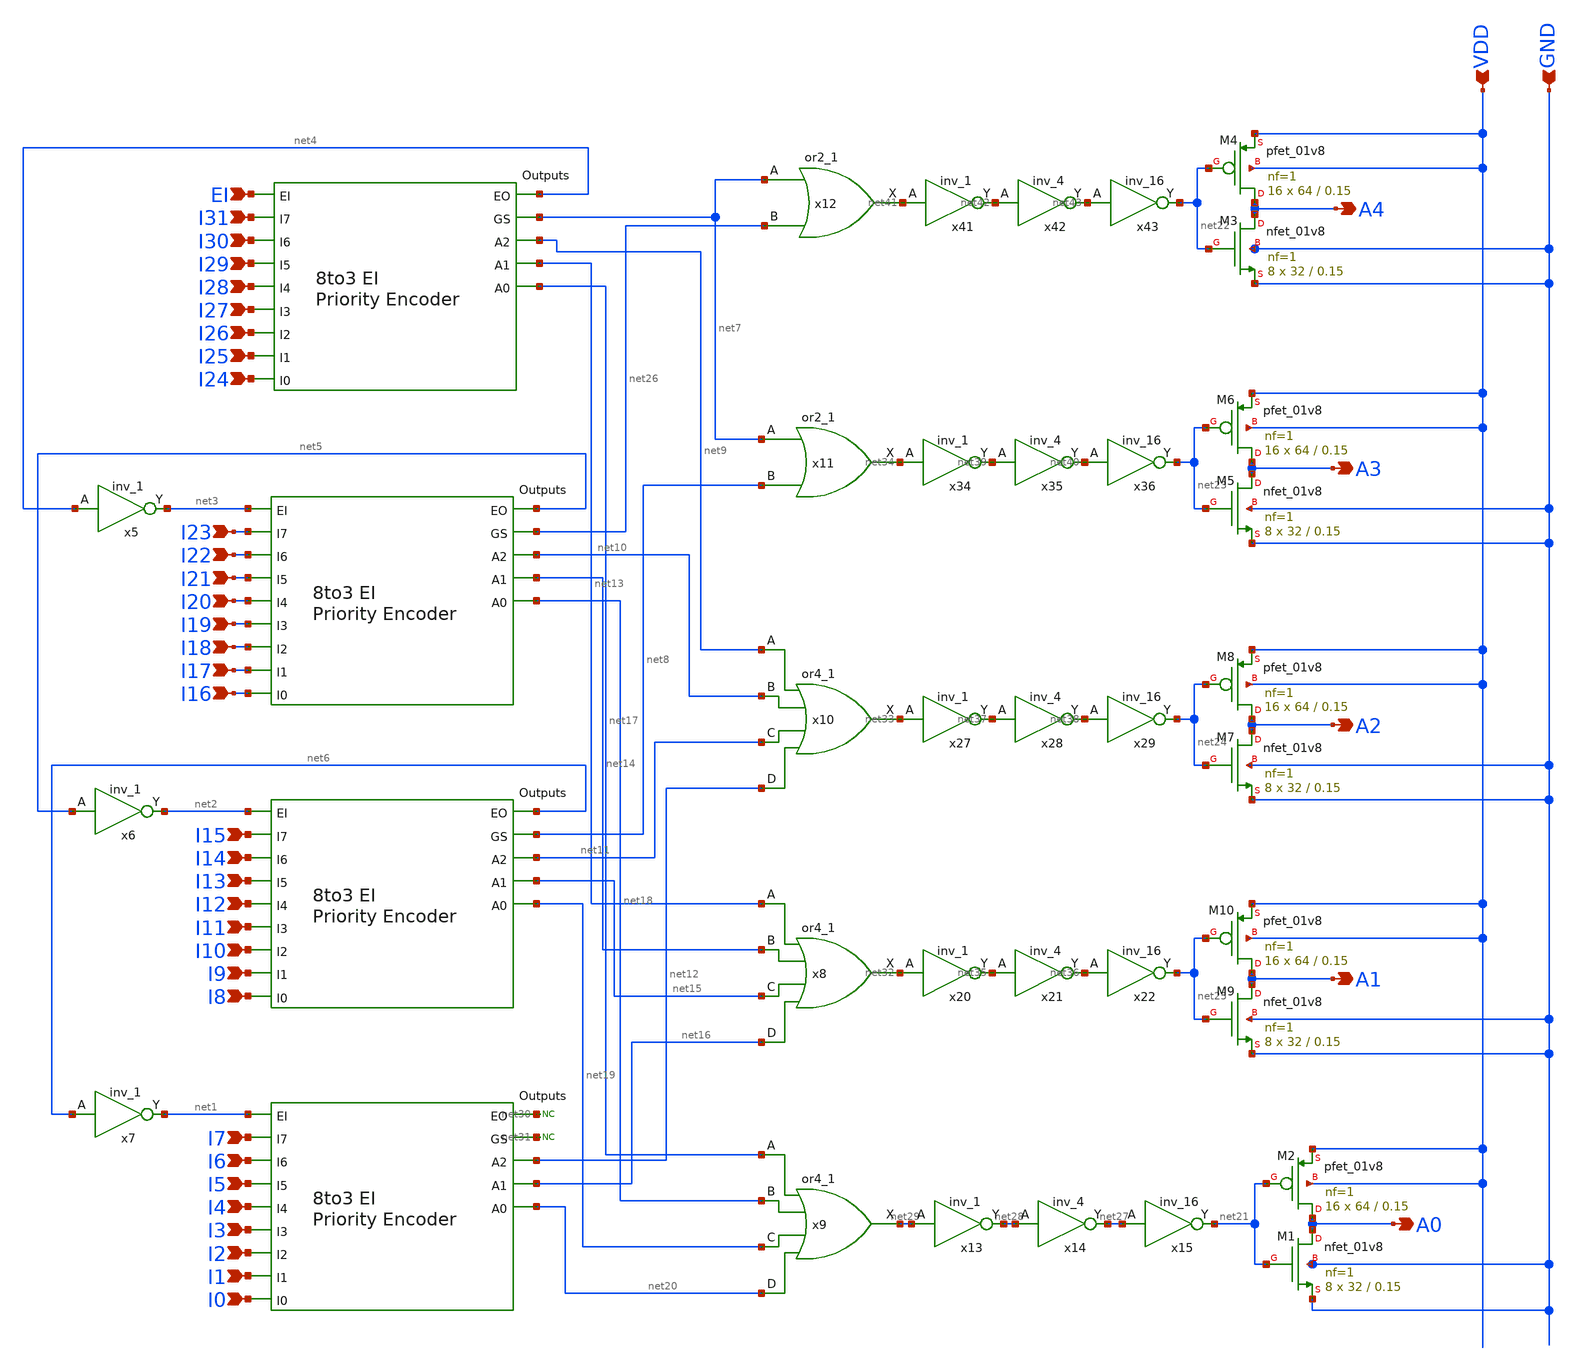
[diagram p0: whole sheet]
** sch_path: PriorityEncoder/xschem/32to5_Priority_Encoder_v0p2p1.sch
.lib $::SKYWATER_MODELS/sky130.lib.spice tt
.include $::SKYWATER_STDCELLS/sky130_fd_sc_hd.spice

**.subckt 32to5_Priority_Encoder_v0p2p1 EI I31 I30 I29 I28 I27 I26 I25 I24 I23 I22 I21 I20 I19 I18
*+ I17 I16 I15 I14 I13 I12 I11 I10 I9 I8 I7 I6 I5 I4 I3 I2 I1 I0 A0 A4 A3 A2 A1 VDD GND
*.ipin EI
*.ipin I31
*.ipin I30
*.ipin I29
*.ipin I28
*.ipin I27
*.ipin I26
*.ipin I25
*.ipin I24
*.ipin I23
*.ipin I22
*.ipin I21
*.ipin I20
*.ipin I19
*.ipin I18
*.ipin I17
*.ipin I16
*.ipin I15
*.ipin I14
*.ipin I13
*.ipin I12
*.ipin I11
*.ipin I10
*.ipin I9
*.ipin I8
*.ipin I7
*.ipin I6
*.ipin I5
*.ipin I4
*.ipin I3
*.ipin I2
*.ipin I1
*.ipin I0
*.opin A0
*.opin A4
*.opin A3
*.opin A2
*.opin A1
*.ipin VDD
*.ipin GND
x1 I25 I29 I27 I24 I26 I30 I31 I28 net4 net7 net9 net13 net17 EI 8to3_Priority_Encoder_v0p2p0
x2 I17 I21 I19 I16 I18 I22 I23 I20 net5 net26 net10 net14 net18 net3 8to3_Priority_Encoder_v0p2p0
x3 I9 I13 I11 I8 I10 I14 I15 I12 net6 net8 net11 net15 net19 net2 8to3_Priority_Encoder_v0p2p0
x4 I1 I5 I3 I0 I2 I6 I7 I4 net30 net31 net12 net16 net20 net1 8to3_Priority_Encoder_v0p2p0
x5 net4 GND GND VDD VDD net3 sky130_fd_sc_hd__inv_1
x9 net17 net18 net19 net20 GND GND VDD VDD net29 sky130_fd_sc_hd__or4_1
x8 net13 net14 net15 net16 GND GND VDD VDD net32 sky130_fd_sc_hd__or4_1
x10 net9 net10 net11 net12 GND GND VDD VDD net33 sky130_fd_sc_hd__or4_1
x11 net7 net8 GND GND VDD VDD net34 sky130_fd_sc_hd__or2_1
x13 net29 GND GND VDD VDD net28 sky130_fd_sc_hd__inv_1
x14 net28 GND GND VDD VDD net27 sky130_fd_sc_hd__inv_4
x15 net27 GND GND VDD VDD net21 sky130_fd_sc_hd__inv_16
x20 net32 GND GND VDD VDD net35 sky130_fd_sc_hd__inv_1
x21 net35 GND GND VDD VDD net36 sky130_fd_sc_hd__inv_4
x22 net36 GND GND VDD VDD net25 sky130_fd_sc_hd__inv_16
x27 net33 GND GND VDD VDD net37 sky130_fd_sc_hd__inv_1
x28 net37 GND GND VDD VDD net38 sky130_fd_sc_hd__inv_4
x29 net38 GND GND VDD VDD net24 sky130_fd_sc_hd__inv_16
x34 net34 GND GND VDD VDD net39 sky130_fd_sc_hd__inv_1
x35 net39 GND GND VDD VDD net40 sky130_fd_sc_hd__inv_4
x36 net40 GND GND VDD VDD net23 sky130_fd_sc_hd__inv_16
x12 net7 net26 GND GND VDD VDD net41 sky130_fd_sc_hd__or2_1
x41 net41 GND GND VDD VDD net42 sky130_fd_sc_hd__inv_1
x42 net42 GND GND VDD VDD net43 sky130_fd_sc_hd__inv_4
x43 net43 GND GND VDD VDD net22 sky130_fd_sc_hd__inv_16
* noconn #net30
* noconn #net31
XM3 A4 net22 GND GND sky130_fd_pr__nfet_01v8 L=0.15 W=32 nf=1 ad='int((nf+1)/2) * W/nf * 0.29' as='int((nf+2)/2) * W/nf * 0.29'
+ pd='2*int((nf+1)/2) * (W/nf + 0.29)' ps='2*int((nf+2)/2) * (W/nf + 0.29)' nrd='0.29 / W' nrs='0.29 / W'
+ sa=0 sb=0 sd=0 mult=8 m=8
XM4 A4 net22 VDD VDD sky130_fd_pr__pfet_01v8 L=0.15 W=64 nf=1 ad='int((nf+1)/2) * W/nf * 0.29' as='int((nf+2)/2) * W/nf * 0.29'
+ pd='2*int((nf+1)/2) * (W/nf + 0.29)' ps='2*int((nf+2)/2) * (W/nf + 0.29)' nrd='0.29 / W' nrs='0.29 / W'
+ sa=0 sb=0 sd=0 mult=16 m=16
XM5 A3 net23 GND GND sky130_fd_pr__nfet_01v8 L=0.15 W=32 nf=1 ad='int((nf+1)/2) * W/nf * 0.29' as='int((nf+2)/2) * W/nf * 0.29'
+ pd='2*int((nf+1)/2) * (W/nf + 0.29)' ps='2*int((nf+2)/2) * (W/nf + 0.29)' nrd='0.29 / W' nrs='0.29 / W'
+ sa=0 sb=0 sd=0 mult=8 m=8
XM6 A3 net23 VDD VDD sky130_fd_pr__pfet_01v8 L=0.15 W=64 nf=1 ad='int((nf+1)/2) * W/nf * 0.29' as='int((nf+2)/2) * W/nf * 0.29'
+ pd='2*int((nf+1)/2) * (W/nf + 0.29)' ps='2*int((nf+2)/2) * (W/nf + 0.29)' nrd='0.29 / W' nrs='0.29 / W'
+ sa=0 sb=0 sd=0 mult=16 m=16
XM7 A2 net24 GND GND sky130_fd_pr__nfet_01v8 L=0.15 W=32 nf=1 ad='int((nf+1)/2) * W/nf * 0.29' as='int((nf+2)/2) * W/nf * 0.29'
+ pd='2*int((nf+1)/2) * (W/nf + 0.29)' ps='2*int((nf+2)/2) * (W/nf + 0.29)' nrd='0.29 / W' nrs='0.29 / W'
+ sa=0 sb=0 sd=0 mult=8 m=8
XM8 A2 net24 VDD VDD sky130_fd_pr__pfet_01v8 L=0.15 W=64 nf=1 ad='int((nf+1)/2) * W/nf * 0.29' as='int((nf+2)/2) * W/nf * 0.29'
+ pd='2*int((nf+1)/2) * (W/nf + 0.29)' ps='2*int((nf+2)/2) * (W/nf + 0.29)' nrd='0.29 / W' nrs='0.29 / W'
+ sa=0 sb=0 sd=0 mult=16 m=16
XM9 A1 net25 GND GND sky130_fd_pr__nfet_01v8 L=0.15 W=32 nf=1 ad='int((nf+1)/2) * W/nf * 0.29' as='int((nf+2)/2) * W/nf * 0.29'
+ pd='2*int((nf+1)/2) * (W/nf + 0.29)' ps='2*int((nf+2)/2) * (W/nf + 0.29)' nrd='0.29 / W' nrs='0.29 / W'
+ sa=0 sb=0 sd=0 mult=8 m=8
XM10 A1 net25 VDD VDD sky130_fd_pr__pfet_01v8 L=0.15 W=64 nf=1 ad='int((nf+1)/2) * W/nf * 0.29' as='int((nf+2)/2) * W/nf * 0.29'
+ pd='2*int((nf+1)/2) * (W/nf + 0.29)' ps='2*int((nf+2)/2) * (W/nf + 0.29)' nrd='0.29 / W' nrs='0.29 / W'
+ sa=0 sb=0 sd=0 mult=16 m=16
XM1 A0 net21 GND GND sky130_fd_pr__nfet_01v8 L=0.15 W=32 nf=1 ad='int((nf+1)/2) * W/nf * 0.29' as='int((nf+2)/2) * W/nf * 0.29'
+ pd='2*int((nf+1)/2) * (W/nf + 0.29)' ps='2*int((nf+2)/2) * (W/nf + 0.29)' nrd='0.29 / W' nrs='0.29 / W'
+ sa=0 sb=0 sd=0 mult=8 m=8
XM2 A0 net21 VDD VDD sky130_fd_pr__pfet_01v8 L=0.15 W=64 nf=1 ad='int((nf+1)/2) * W/nf * 0.29' as='int((nf+2)/2) * W/nf * 0.29'
+ pd='2*int((nf+1)/2) * (W/nf + 0.29)' ps='2*int((nf+2)/2) * (W/nf + 0.29)' nrd='0.29 / W' nrs='0.29 / W'
+ sa=0 sb=0 sd=0 mult=16 m=16
x6 net5 GND GND VDD VDD net2 sky130_fd_sc_hd__inv_1
x7 net6 GND GND VDD VDD net1 sky130_fd_sc_hd__inv_1
**.ends
.end
